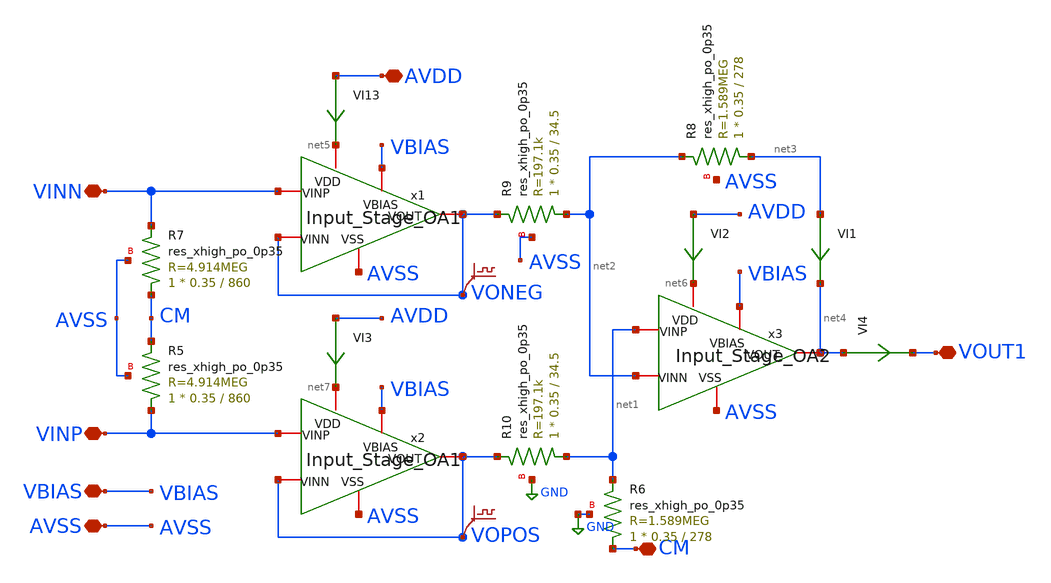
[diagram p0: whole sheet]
** sch_path: xschem/Input_Stage_v1.sch
**.subckt Input_Stage_v1 VINP CM VINN VOUT1 AVDD AVSS VBIAS
*.iopin VINP
*.iopin CM
*.iopin VINN
*.iopin VOUT1
*.iopin AVDD
*.iopin AVSS
*.iopin VBIAS
VI13 AVDD net5 0
.save i(vi13)
VI2 AVDD net6 0
.save i(vi2)
VI3 AVDD net7 0
.save i(vi3)
.save v(voneg)
.save v(vopos)
VI1 net3 net4 0
.save i(vi1)
VI4 net4 VOUT1 0
.save i(vi4)
x1 net5 VONEG VONEG VINN VBIAS AVSS Input_Stage_OA1
x2 net7 VOPOS VOPOS VINP VBIAS AVSS Input_Stage_OA1
x3 net6 net4 net2 net1 VBIAS AVSS Input_Stage_OA2
XR7 CM VINN AVSS sky130_fd_pr__res_xhigh_po_0p35 L=860 mult=1 m=1
XR5 VINP CM AVSS sky130_fd_pr__res_xhigh_po_0p35 L=860 mult=1 m=1
XR6 CM net1 GND sky130_fd_pr__res_xhigh_po_0p35 L=278 mult=1 m=1
XR8 net3 net2 AVSS sky130_fd_pr__res_xhigh_po_0p35 L=278 mult=1 m=1
XR9 net2 VONEG AVSS sky130_fd_pr__res_xhigh_po_0p35 L=34.5 mult=1 m=1
XR10 net1 VOPOS GND sky130_fd_pr__res_xhigh_po_0p35 L=34.5 mult=1 m=1
**.ends

* expanding   symbol:  Input_Stage_OA1.sym # of pins=6
** sym_path: xschem/Input_Stage_OA1.sym
** sch_path: xschem/Input_Stage_OA1.sch
.subckt Input_Stage_OA1 VDD VOUT VINN VINP VBIAS VSS
*.iopin VINN
*.iopin VINP
*.iopin VOUT
*.iopin VDD
*.iopin VSS
*.iopin VBIAS
XM1 net4 VINN net1 net1 sky130_fd_pr__nfet_01v8_lvt L=0.15 W=7.5 nf=1 ad='int((nf+1)/2) * W/nf * 0.29'
+ as='int((nf+2)/2) * W/nf * 0.29' pd='2*int((nf+1)/2) * (W/nf + 0.29)' ps='2*int((nf+2)/2) * (W/nf + 0.29)'
+ nrd='0.29 / W' nrs='0.29 / W' sa=0 sb=0 sd=0 mult=1 m=1
XM2 net3 VINP net1 net1 sky130_fd_pr__nfet_01v8_lvt L=0.15 W=7.5 nf=1 ad='int((nf+1)/2) * W/nf * 0.29'
+ as='int((nf+2)/2) * W/nf * 0.29' pd='2*int((nf+1)/2) * (W/nf + 0.29)' ps='2*int((nf+2)/2) * (W/nf + 0.29)'
+ nrd='0.29 / W' nrs='0.29 / W' sa=0 sb=0 sd=0 mult=1 m=1
VISink net1 net2 0
.save i(visink)
XM6 net5 net5 net6 net6 sky130_fd_pr__pfet_01v8_lvt L=5 W=20 nf=1 ad='int((nf+1)/2) * W/nf * 0.29' as='int((nf+2)/2) * W/nf * 0.29'
+ pd='2*int((nf+1)/2) * (W/nf + 0.29)' ps='2*int((nf+2)/2) * (W/nf + 0.29)' nrd='0.29 / W' nrs='0.29 / W'
+ sa=0 sb=0 sd=0 mult=2 m=2
XM7 net7 net5 net6 net6 sky130_fd_pr__pfet_01v8_lvt L=5 W=20 nf=1 ad='int((nf+1)/2) * W/nf * 0.29' as='int((nf+2)/2) * W/nf * 0.29'
+ pd='2*int((nf+1)/2) * (W/nf + 0.29)' ps='2*int((nf+2)/2) * (W/nf + 0.29)' nrd='0.29 / W' nrs='0.29 / W'
+ sa=0 sb=0 sd=0 mult=2 m=2
VD1 net5 net8 0
.save i(vd1)
VID2 net7 net9 0
.save i(vid2)
VID1 VOUT net12 0
.save i(vid1)
VID3 net11 VOUT 0
.save i(vid3)
.save v(vinn)
.save v(vinp)
.save v(vout)
VIBIAS VBIAS net10 0
.save i(vibias)
XM10 net8 VINN net4 net4 sky130_fd_pr__nfet_05v0_nvt L=2 W=1 nf=1 ad='int((nf+1)/2) * W/nf * 0.29' as='int((nf+2)/2) * W/nf * 0.29'
+ pd='2*int((nf+1)/2) * (W/nf + 0.29)' ps='2*int((nf+2)/2) * (W/nf + 0.29)' nrd='0.29 / W' nrs='0.29 / W'
+ sa=0 sb=0 sd=0 mult=25 m=25
XM12 net9 VINP net3 net3 sky130_fd_pr__nfet_05v0_nvt L=2 W=1 nf=1 ad='int((nf+1)/2) * W/nf * 0.29' as='int((nf+2)/2) * W/nf * 0.29'
+ pd='2*int((nf+1)/2) * (W/nf + 0.29)' ps='2*int((nf+2)/2) * (W/nf + 0.29)' nrd='0.29 / W' nrs='0.29 / W'
+ sa=0 sb=0 sd=0 mult=25 m=25
XM3 net2 net10 VSS VSS sky130_fd_pr__nfet_g5v0d10v5 L=1 W=5 nf=1 ad='int((nf+1)/2) * W/nf * 0.29' as='int((nf+2)/2) * W/nf * 0.29'
+ pd='2*int((nf+1)/2) * (W/nf + 0.29)' ps='2*int((nf+2)/2) * (W/nf + 0.29)' nrd='0.29 / W' nrs='0.29 / W'
+ sa=0 sb=0 sd=0 mult=10 m=10
XM5 net12 net10 VSS VSS sky130_fd_pr__nfet_g5v0d10v5 L=1 W=5 nf=1 ad='int((nf+1)/2) * W/nf * 0.29' as='int((nf+2)/2) * W/nf * 0.29'
+ pd='2*int((nf+1)/2) * (W/nf + 0.29)' ps='2*int((nf+2)/2) * (W/nf + 0.29)' nrd='0.29 / W' nrs='0.29 / W'
+ sa=0 sb=0 sd=0 mult=20 m=20
XM8 net11 net7 net6 net6 sky130_fd_pr__pfet_g5v0d10v5 L=0.5 W=10 nf=1 ad='int((nf+1)/2) * W/nf * 0.29'
+ as='int((nf+2)/2) * W/nf * 0.29' pd='2*int((nf+1)/2) * (W/nf + 0.29)' ps='2*int((nf+2)/2) * (W/nf + 0.29)'
+ nrd='0.29 / W' nrs='0.29 / W' sa=0 sb=0 sd=0 mult=10 m=10
VIVDD VDD net6 0
.save i(vivdd)
XC1 net7 net13 sky130_fd_pr__cap_mim_m3_1 W=10 L=10 MF=15 m=15
XR2 net13 VOUT VSS sky130_fd_pr__res_high_po_0p69 L=41 mult=1 m=1
.ends


* expanding   symbol:  Input_Stage_OA2.sym # of pins=6
** sym_path: xschem/Input_Stage_OA2.sym
** sch_path: xschem/Input_Stage_OA2.sch
.subckt Input_Stage_OA2 VDD VOUT VINN VINP VBIAS VSS
*.iopin VINN
*.iopin VINP
*.iopin VOUT
*.iopin VDD
*.iopin VSS
*.iopin VBIAS
XM1 net4 VINN net1 net1 sky130_fd_pr__nfet_01v8_lvt L=0.15 W=7.5 nf=1 ad='int((nf+1)/2) * W/nf * 0.29'
+ as='int((nf+2)/2) * W/nf * 0.29' pd='2*int((nf+1)/2) * (W/nf + 0.29)' ps='2*int((nf+2)/2) * (W/nf + 0.29)'
+ nrd='0.29 / W' nrs='0.29 / W' sa=0 sb=0 sd=0 mult=1 m=1
XM2 net3 VINP net1 net1 sky130_fd_pr__nfet_01v8_lvt L=0.15 W=7.5 nf=1 ad='int((nf+1)/2) * W/nf * 0.29'
+ as='int((nf+2)/2) * W/nf * 0.29' pd='2*int((nf+1)/2) * (W/nf + 0.29)' ps='2*int((nf+2)/2) * (W/nf + 0.29)'
+ nrd='0.29 / W' nrs='0.29 / W' sa=0 sb=0 sd=0 mult=1 m=1
VISink net1 net2 0
.save i(visink)
XM6 net5 net5 net6 net6 sky130_fd_pr__pfet_01v8_lvt L=5 W=20 nf=1 ad='int((nf+1)/2) * W/nf * 0.29' as='int((nf+2)/2) * W/nf * 0.29'
+ pd='2*int((nf+1)/2) * (W/nf + 0.29)' ps='2*int((nf+2)/2) * (W/nf + 0.29)' nrd='0.29 / W' nrs='0.29 / W'
+ sa=0 sb=0 sd=0 mult=2 m=2
XM7 net7 net5 net6 net6 sky130_fd_pr__pfet_01v8_lvt L=5 W=20 nf=1 ad='int((nf+1)/2) * W/nf * 0.29' as='int((nf+2)/2) * W/nf * 0.29'
+ pd='2*int((nf+1)/2) * (W/nf + 0.29)' ps='2*int((nf+2)/2) * (W/nf + 0.29)' nrd='0.29 / W' nrs='0.29 / W'
+ sa=0 sb=0 sd=0 mult=2 m=2
VD1 net5 net8 0
.save i(vd1)
VID2 net7 net9 0
.save i(vid2)
VID1 VOUT net12 0
.save i(vid1)
VID3 net11 VOUT 0
.save i(vid3)
.save v(vinn)
.save v(vinp)
.save v(vout)
VIBIAS VBIAS net10 0
.save i(vibias)
XM10 net8 VINN net4 net4 sky130_fd_pr__nfet_05v0_nvt L=2 W=1 nf=1 ad='int((nf+1)/2) * W/nf * 0.29' as='int((nf+2)/2) * W/nf * 0.29'
+ pd='2*int((nf+1)/2) * (W/nf + 0.29)' ps='2*int((nf+2)/2) * (W/nf + 0.29)' nrd='0.29 / W' nrs='0.29 / W'
+ sa=0 sb=0 sd=0 mult=25 m=25
XM12 net9 VINP net3 net3 sky130_fd_pr__nfet_05v0_nvt L=2 W=1 nf=1 ad='int((nf+1)/2) * W/nf * 0.29' as='int((nf+2)/2) * W/nf * 0.29'
+ pd='2*int((nf+1)/2) * (W/nf + 0.29)' ps='2*int((nf+2)/2) * (W/nf + 0.29)' nrd='0.29 / W' nrs='0.29 / W'
+ sa=0 sb=0 sd=0 mult=25 m=25
XM3 net2 net10 VSS VSS sky130_fd_pr__nfet_g5v0d10v5 L=1 W=5 nf=1 ad='int((nf+1)/2) * W/nf * 0.29' as='int((nf+2)/2) * W/nf * 0.29'
+ pd='2*int((nf+1)/2) * (W/nf + 0.29)' ps='2*int((nf+2)/2) * (W/nf + 0.29)' nrd='0.29 / W' nrs='0.29 / W'
+ sa=0 sb=0 sd=0 mult=20 m=20
XM5 net12 net10 VSS VSS sky130_fd_pr__nfet_g5v0d10v5 L=1 W=5 nf=1 ad='int((nf+1)/2) * W/nf * 0.29' as='int((nf+2)/2) * W/nf * 0.29'
+ pd='2*int((nf+1)/2) * (W/nf + 0.29)' ps='2*int((nf+2)/2) * (W/nf + 0.29)' nrd='0.29 / W' nrs='0.29 / W'
+ sa=0 sb=0 sd=0 mult=100 m=100
XM8 net11 net7 net6 net6 sky130_fd_pr__pfet_g5v0d10v5 L=0.5 W=10 nf=1 ad='int((nf+1)/2) * W/nf * 0.29'
+ as='int((nf+2)/2) * W/nf * 0.29' pd='2*int((nf+1)/2) * (W/nf + 0.29)' ps='2*int((nf+2)/2) * (W/nf + 0.29)'
+ nrd='0.29 / W' nrs='0.29 / W' sa=0 sb=0 sd=0 mult=10 m=10
VIVDD VDD net6 0
.save i(vivdd)
XC1 net7 net13 sky130_fd_pr__cap_mim_m3_1 W=10 L=10 MF=15 m=15
XR1 net13 VOUT VSS sky130_fd_pr__res_high_po_0p69 L=41 mult=1 m=1
.ends

.GLOBAL GND
.end
